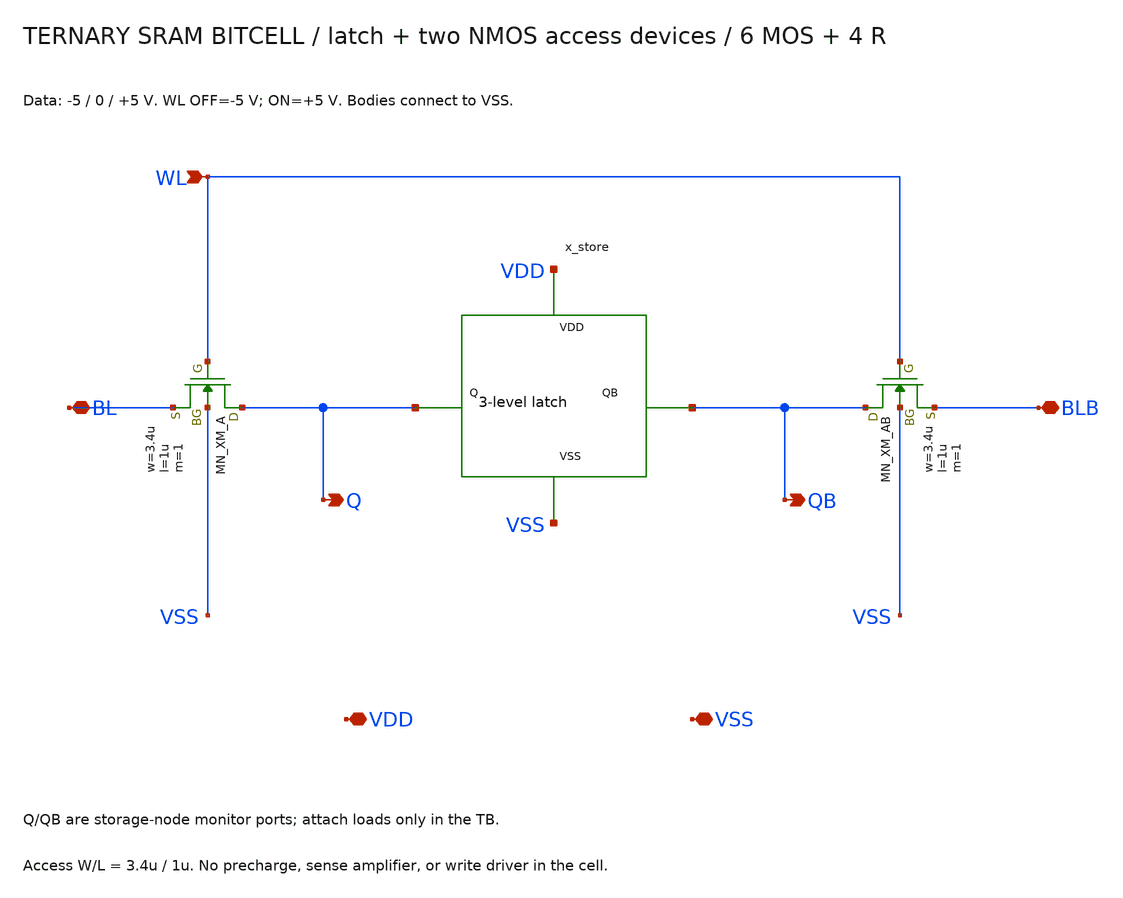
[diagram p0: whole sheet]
** sch_path: member_project/balanced-ternary-logic/PenguinEino/ternary_sram.sch
**.subckt ternary_sram WL BL BLB Q QB VDD VSS
*.ipin WL
*.iopin BL
*.iopin BLB
*.opin Q
*.opin QB
*.iopin VDD
*.iopin VSS
x_store Q QB VDD VSS ternary_latch
XXM_A Q WL BL VSS NMOS w=3.4u l=1u nrd=0 nrs=0 m=1
XXM_AB QB WL BLB VSS NMOS w=3.4u l=1u nrd=0 nrs=0 m=1
**.ends

* expanding   symbol:  /home/ishi-kai/balanced-ternary-logic/ternary_latch.sym # of pins=4
** sym_path: member_project/balanced-ternary-logic/PenguinEino/ternary_latch.sym
** sch_path: member_project/balanced-ternary-logic/PenguinEino/ternary_latch.sch
.subckt ternary_latch Q QB VDD VSS
*.opin Q
*.opin QB
*.iopin VDD
*.iopin VSS
x_q QB Q VDD VSS inverter
x_qb Q QB VDD VSS inverter
.ends


* expanding   symbol:  /home/ishi-kai/balanced-ternary-logic/inverter.sym # of pins=4
** sym_path: member_project/balanced-ternary-logic/PenguinEino/inverter.sym
** sch_path: member_project/balanced-ternary-logic/PenguinEino/inverter.sch
.subckt inverter vin vout VDD VSS
*.iopin VDD
*.ipin vin
*.opin vout
*.iopin VSS
XXM1 net1 vin VDD VDD PMOS w=13.5u l=1u nrd=0 nrs=0 m=1
XR1 net1 vout VDD F_RR w=2.8e-06 l=30e-06 R=1 tc1=0 tc2=0 m=1
XR2 vout net2 VDD F_RR w=2.8e-06 l=30e-06 R=1 tc1=0 tc2=0 m=1
XXM2 net2 vin VSS VSS NMOS w=5u l=1u nrd=0 nrs=0 m=1
.ends

.end
